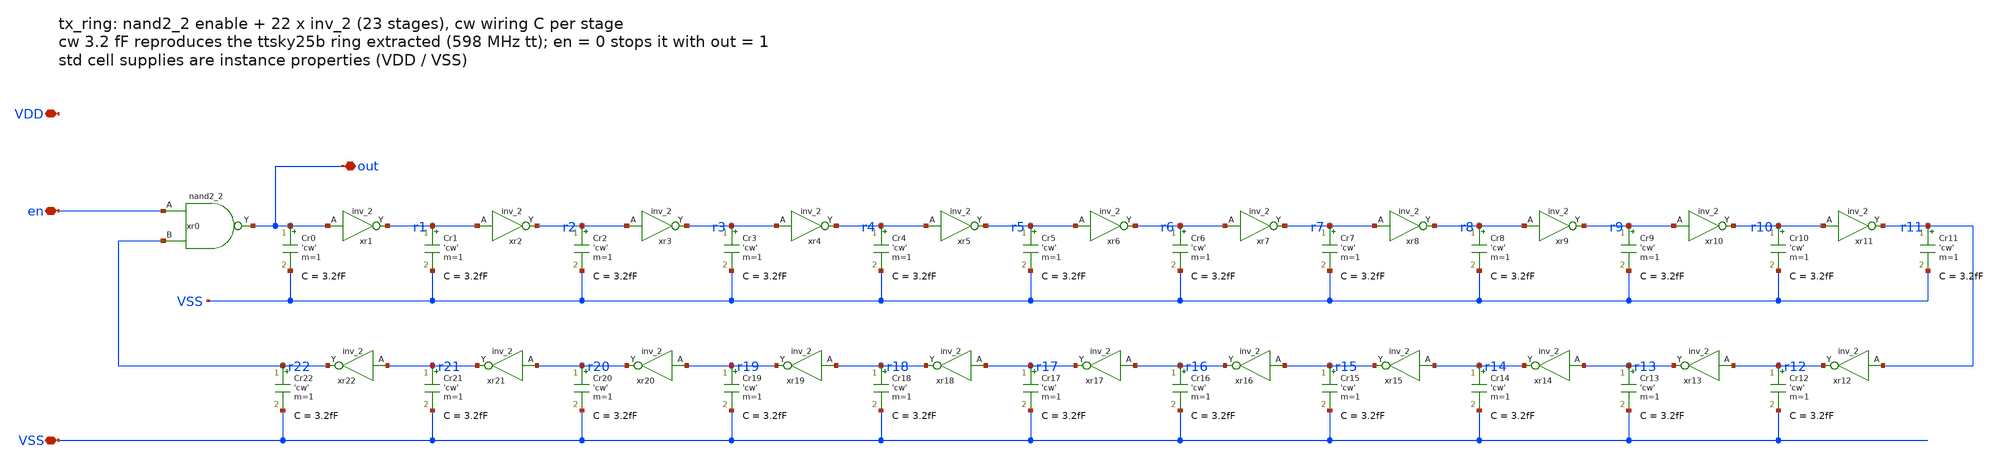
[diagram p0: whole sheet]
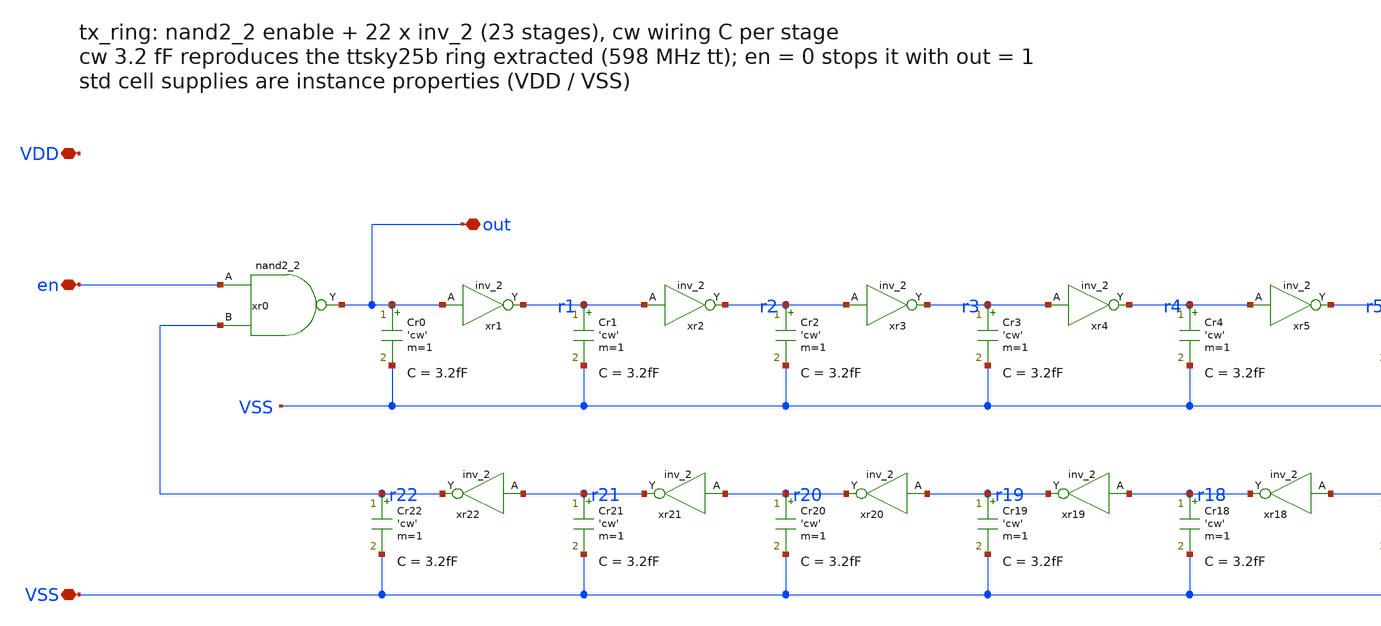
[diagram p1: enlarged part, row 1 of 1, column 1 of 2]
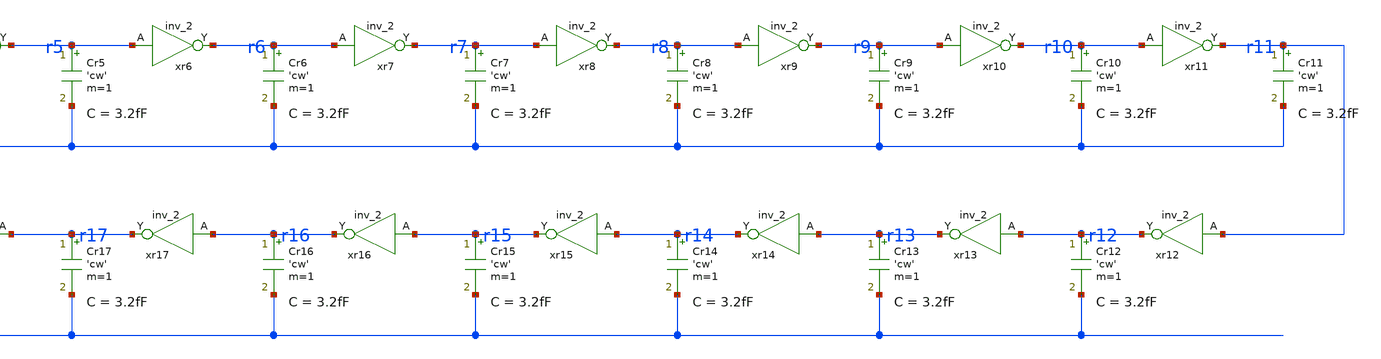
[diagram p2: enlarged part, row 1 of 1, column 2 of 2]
** sch_path: xschem/tx_ring.sch
**.subckt tx_ring VDD VSS en out
*.iopin VDD
*.iopin VSS
*.iopin en
*.iopin out
xr0 en r22 VSS VSS VDD VDD out sky130_fd_sc_hd__nand2_2
Cr0 out VSS 'cw' m=1
xr1 out VSS VSS VDD VDD r1 sky130_fd_sc_hd__inv_2
Cr1 r1 VSS 'cw' m=1
xr2 r1 VSS VSS VDD VDD r2 sky130_fd_sc_hd__inv_2
Cr2 r2 VSS 'cw' m=1
xr3 r2 VSS VSS VDD VDD r3 sky130_fd_sc_hd__inv_2
Cr3 r3 VSS 'cw' m=1
xr4 r3 VSS VSS VDD VDD r4 sky130_fd_sc_hd__inv_2
Cr4 r4 VSS 'cw' m=1
xr5 r4 VSS VSS VDD VDD r5 sky130_fd_sc_hd__inv_2
Cr5 r5 VSS 'cw' m=1
xr6 r5 VSS VSS VDD VDD r6 sky130_fd_sc_hd__inv_2
Cr6 r6 VSS 'cw' m=1
xr7 r6 VSS VSS VDD VDD r7 sky130_fd_sc_hd__inv_2
Cr7 r7 VSS 'cw' m=1
xr8 r7 VSS VSS VDD VDD r8 sky130_fd_sc_hd__inv_2
Cr8 r8 VSS 'cw' m=1
xr9 r8 VSS VSS VDD VDD r9 sky130_fd_sc_hd__inv_2
Cr9 r9 VSS 'cw' m=1
xr10 r9 VSS VSS VDD VDD r10 sky130_fd_sc_hd__inv_2
Cr10 r10 VSS 'cw' m=1
xr11 r10 VSS VSS VDD VDD r11 sky130_fd_sc_hd__inv_2
Cr11 r11 VSS 'cw' m=1
xr12 r11 VSS VSS VDD VDD r12 sky130_fd_sc_hd__inv_2
Cr12 r12 VSS 'cw' m=1
xr13 r12 VSS VSS VDD VDD r13 sky130_fd_sc_hd__inv_2
Cr13 r13 VSS 'cw' m=1
xr14 r13 VSS VSS VDD VDD r14 sky130_fd_sc_hd__inv_2
Cr14 r14 VSS 'cw' m=1
xr15 r14 VSS VSS VDD VDD r15 sky130_fd_sc_hd__inv_2
Cr15 r15 VSS 'cw' m=1
xr16 r15 VSS VSS VDD VDD r16 sky130_fd_sc_hd__inv_2
Cr16 r16 VSS 'cw' m=1
xr17 r16 VSS VSS VDD VDD r17 sky130_fd_sc_hd__inv_2
Cr17 r17 VSS 'cw' m=1
xr18 r17 VSS VSS VDD VDD r18 sky130_fd_sc_hd__inv_2
Cr18 r18 VSS 'cw' m=1
xr19 r18 VSS VSS VDD VDD r19 sky130_fd_sc_hd__inv_2
Cr19 r19 VSS 'cw' m=1
xr20 r19 VSS VSS VDD VDD r20 sky130_fd_sc_hd__inv_2
Cr20 r20 VSS 'cw' m=1
xr21 r20 VSS VSS VDD VDD r21 sky130_fd_sc_hd__inv_2
Cr21 r21 VSS 'cw' m=1
xr22 r21 VSS VSS VDD VDD r22 sky130_fd_sc_hd__inv_2
Cr22 r22 VSS 'cw' m=1
**.ends
.end
